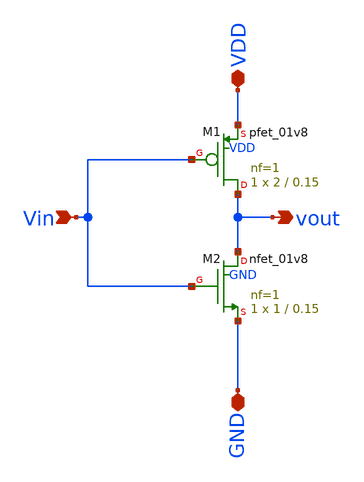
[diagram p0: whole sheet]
** sch_path: pll/pfd_cp_lf_lib/inverter/xschem/inverter.sch
**.subckt inverter Vin VDD GND vout
*.ipin Vin
*.iopin VDD
*.iopin GND
*.opin vout
XM2 vout Vin GND GND sky130_fd_pr__nfet_01v8 L=0.15 W=1 nf=1 ad='int((nf+1)/2) * W/nf * 0.29' as='int((nf+2)/2) * W/nf * 0.29'
+ pd='2*int((nf+1)/2) * (W/nf + 0.29)' ps='2*int((nf+2)/2) * (W/nf + 0.29)' nrd='0.29 / W' nrs='0.29 / W'
+ sa=0 sb=0 sd=0 mult=1 m=1
XM1 vout Vin VDD VDD sky130_fd_pr__pfet_01v8 L=0.15 W=2 nf=1 ad='int((nf+1)/2) * W/nf * 0.29' as='int((nf+2)/2) * W/nf * 0.29'
+ pd='2*int((nf+1)/2) * (W/nf + 0.29)' ps='2*int((nf+2)/2) * (W/nf + 0.29)' nrd='0.29 / W' nrs='0.29 / W'
+ sa=0 sb=0 sd=0 mult=1 m=1
**.ends
.end
